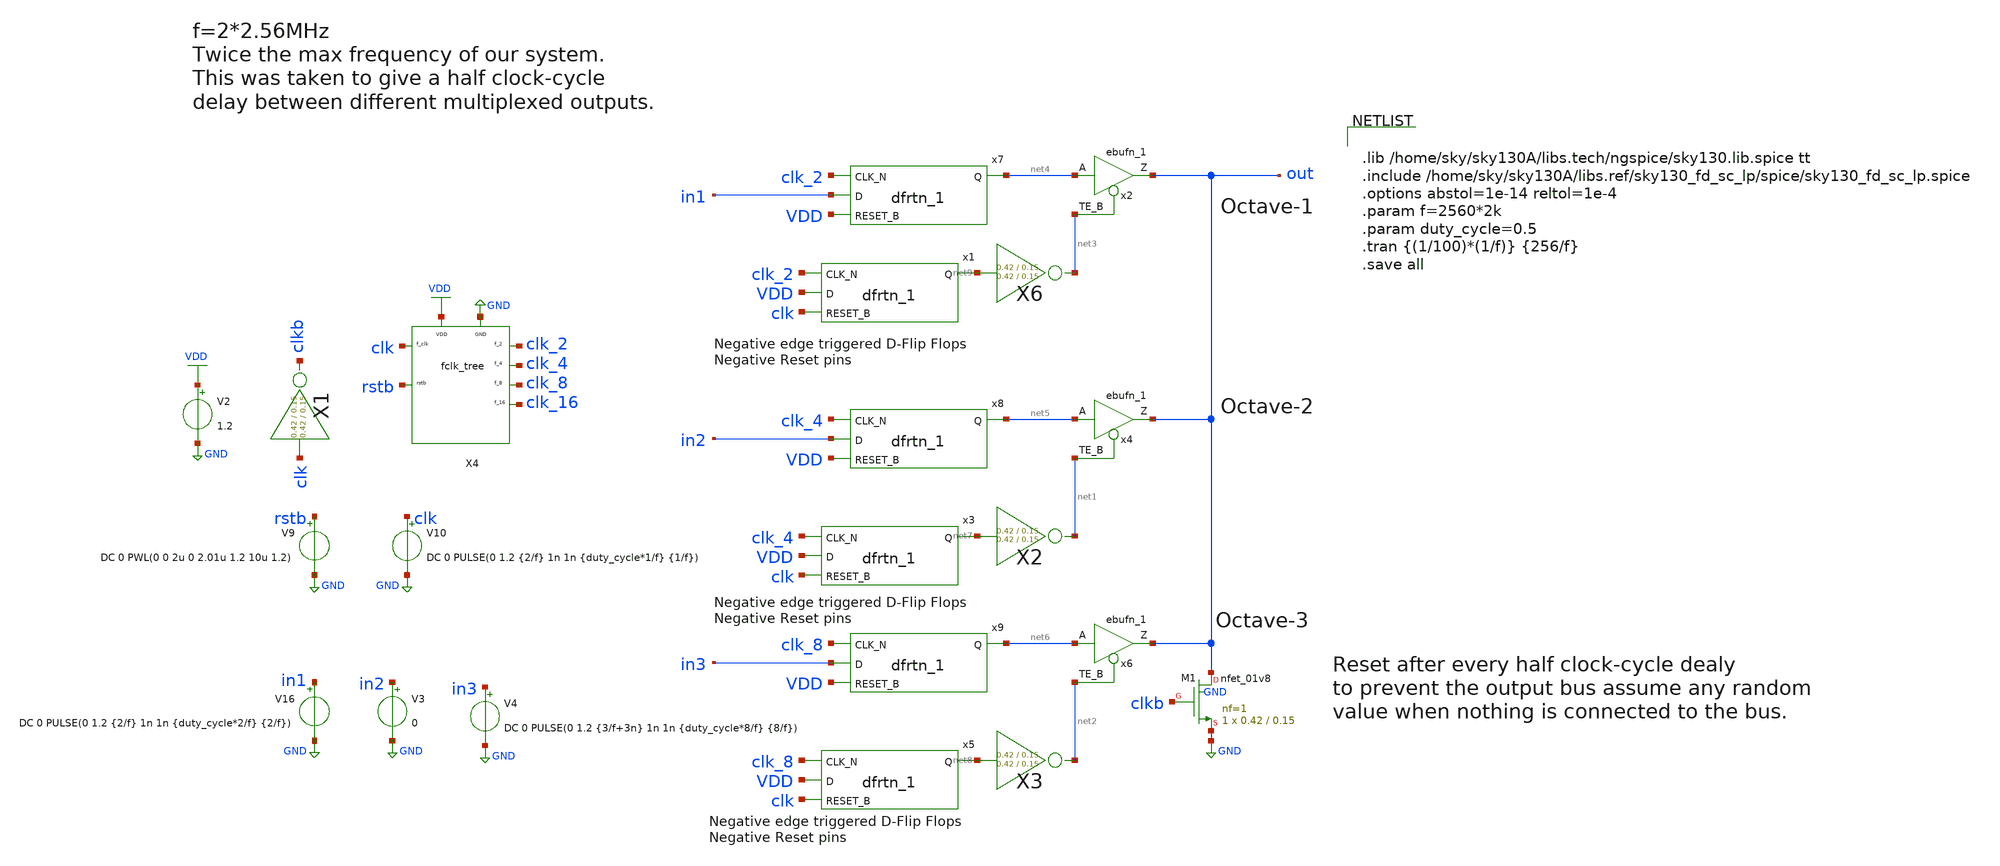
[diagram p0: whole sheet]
** sch_path: xschem/readout/sample_ro.sch
**.subckt sample_ro
X2 net7 net1 inv Wpmos=0.42 Lpmos=0.15 Wnmos=0.42 Lnmos=0.15
X3 net8 net2 inv Wpmos=0.42 Lpmos=0.15 Wnmos=0.42 Lnmos=0.15
V2 VDD GND 1.2
X4 clk rstb clk_2 clk_4 VDD GND clk_8 clk_16 fclk_tree
x3 clk_4 VDD clk GND GND VDD VDD net7 sky130_fd_sc_lp__dfrtn_1
x5 clk_8 VDD clk GND GND VDD VDD net8 sky130_fd_sc_lp__dfrtn_1
V10 clk GND DC 0 PULSE(0 1.2 {2/f} 1n 1n {duty_cycle*1/f} {1/f})
x4 net5 net1 GND GND VDD VDD out sky130_fd_sc_lp__ebufn_1
x6 net6 net2 GND GND VDD VDD out sky130_fd_sc_lp__ebufn_1
V9 rstb GND DC 0 PWL(0 0 2u 0 2.01u 1.2 10u 1.2)
X6 net9 net3 inv Wpmos=0.42 Lpmos=0.15 Wnmos=0.42 Lnmos=0.15
x1 clk_2 VDD clk GND GND VDD VDD net9 sky130_fd_sc_lp__dfrtn_1
x2 net4 net3 GND GND VDD VDD out sky130_fd_sc_lp__ebufn_1
XM1 out clkb GND GND sky130_fd_pr__nfet_01v8 L=0.15 W=0.42 nf=1 ad='int((nf+1)/2) * W/nf * 0.29' as='int((nf+2)/2) * W/nf * 0.29'
+ pd='2*int((nf+1)/2) * (W/nf + 0.29)' ps='2*int((nf+2)/2) * (W/nf + 0.29)' nrd='0.29 / W' nrs='0.29 / W'
+ sa=0 sb=0 sd=0 mult=1 m=1
X1 clk clkb inv Wpmos=0.42 Lpmos=0.15 Wnmos=0.42 Lnmos=0.15
V16 in1 GND DC 0 PULSE(0 1.2 {2/f} 1n 1n {duty_cycle*2/f} {2/f})
V3 in2 GND 0
V4 in3 GND DC 0 PULSE(0 1.2 {3/f+3n} 1n 1n {duty_cycle*8/f} {8/f})
x7 clk_2 in1 VDD GND GND VDD VDD net4 sky130_fd_sc_lp__dfrtn_1
x8 clk_4 in2 VDD GND GND VDD VDD net5 sky130_fd_sc_lp__dfrtn_1
x9 clk_8 in3 VDD GND GND VDD VDD net6 sky130_fd_sc_lp__dfrtn_1
**** begin user architecture code


.lib /home/sky/sky130A/libs.tech/ngspice/sky130.lib.spice tt
.include /home/sky/sky130A/libs.ref/sky130_fd_sc_lp/spice/sky130_fd_sc_lp.spice
.options abstol=1e-14 reltol=1e-4
.param f=2560*2k
.param duty_cycle=0.5
.tran {(1/100)*(1/f)} {256/f}
.save all


**** end user architecture code
**.ends

* expanding   symbol:  inv/inv.sym # of pins=2
** sym_path: xschem/inv/inv.sym
** sch_path: xschem/inv/inv.sch
.subckt inv in out  Wpmos=3 Lpmos=0.18 Wnmos=1 Lnmos=0.18
*.ipin in
*.iopin out
XM1 out in GND GND sky130_fd_pr__nfet_01v8 L=Lnmos W=Wnmos nf=1 ad='int((nf+1)/2) * W/nf * 0.29' as='int((nf+2)/2) * W/nf * 0.29'
+ pd='2*int((nf+1)/2) * (W/nf + 0.29)' ps='2*int((nf+2)/2) * (W/nf + 0.29)' nrd='0.29 / W' nrs='0.29 / W'
+ sa=0 sb=0 sd=0 mult=1 m=1
XM2 out in VDD VDD sky130_fd_pr__pfet_01v8 L=Lpmos W=Wpmos nf=1 ad='int((nf+1)/2) * W/nf * 0.29' as='int((nf+2)/2) * W/nf * 0.29'
+ pd='2*int((nf+1)/2) * (W/nf + 0.29)' ps='2*int((nf+2)/2) * (W/nf + 0.29)' nrd='0.29 / W' nrs='0.29 / W'
+ sa=0 sb=0 sd=0 mult=1 m=1
.ends


* expanding   symbol:  readout/fclk_tree.sym # of pins=8
** sym_path: xschem/readout/fclk_tree.sym
** sch_path: xschem/readout/fclk_tree.sch
.subckt fclk_tree f_clk rstb f_2 f_4 VDD GND f_8 f_16
*.iopin VDD
*.iopin GND
*.ipin rstb
*.opin f_2
*.opin f_4
*.opin f_8
*.opin f_16
*.ipin f_clk
x2 f_clk net1 rstb gnd gnd vdd vdd f_2 net1 sky130_fd_sc_lp__dfrbp_1
x4 f_2 net2 rstb gnd gnd vdd vdd f_4 net2 sky130_fd_sc_lp__dfrbp_1
x1 f_4 net3 rstb gnd gnd vdd vdd f_8 net3 sky130_fd_sc_lp__dfrbp_1
x6 f_8 net4 rstb gnd gnd vdd vdd f_16 net4 sky130_fd_sc_lp__dfrbp_1
.ends

.GLOBAL GND
.GLOBAL VDD
.end
